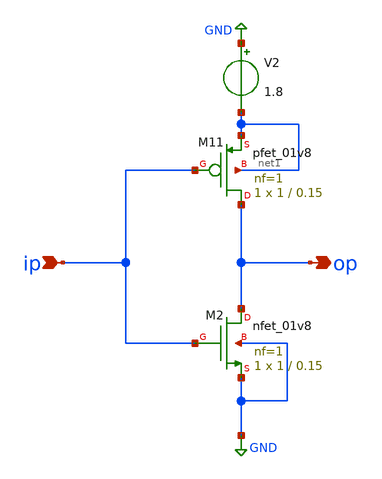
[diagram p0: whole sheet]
** sch_path: ANALOG_PERIPHERAL/DAC/schematic/inverter.sch
**.subckt inverter ip op
*.ipin ip
*.opin op
XM2 op ip GND GND sky130_fd_pr__nfet_01v8 L=0.15 W=1 nf=1 ad='int((1 + 1)/2) * 1 / 1 * 0.29' as='int((1 + 2)/2) * 1 / 1 * 0.29'
+ pd='2*int((1 + 1)/2) * (1 / 1 + 0.29)' ps='2*int((1 + 2)/2) * (1 / 1 + 0.29)' nrd='0.29 / 1 ' nrs='0.29 / 1 '
+ sa=0 sb=0 sd=0 mult=1 m=1
V2 GND net1 1.8
XM11 op ip net1 net1 sky130_fd_pr__pfet_01v8 L=0.15 W=1 nf=1 ad='int((nf+1)/2) * W/nf * 0.29' as='int((nf+2)/2) * W/nf * 0.29'
+ pd='2*int((nf+1)/2) * (W/nf + 0.29)' ps='2*int((nf+2)/2) * (W/nf + 0.29)' nrd='0.29 / W' nrs='0.29 / W'
+ sa=0 sb=0 sd=0 mult=1 m=1
**.ends
.GLOBAL GND
.end
